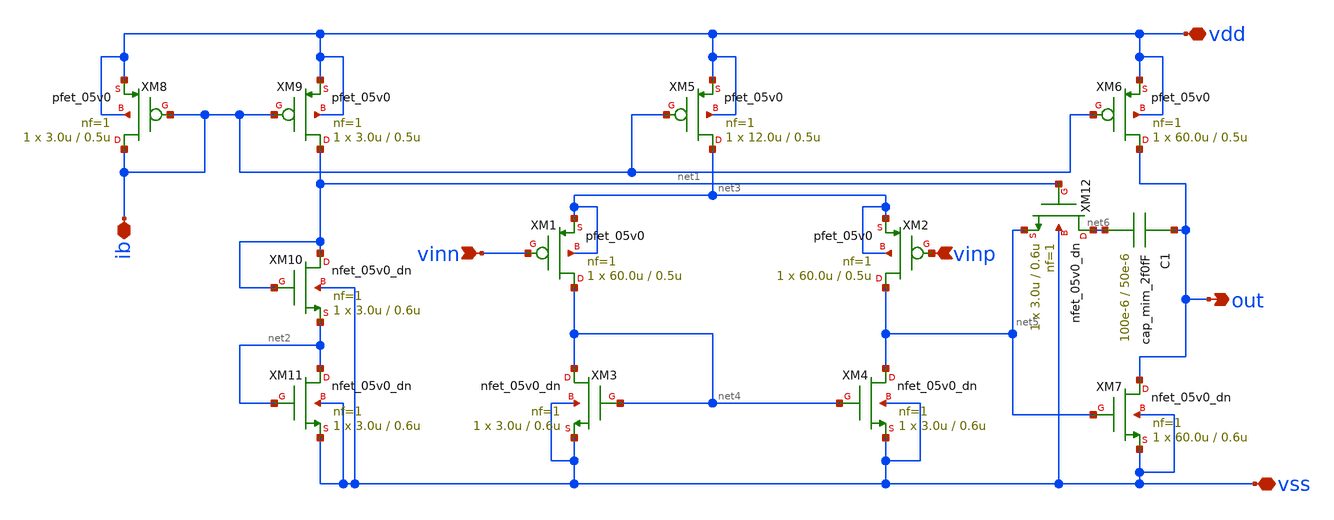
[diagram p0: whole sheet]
** sch_path: member_project/yamada3/opamp_2L_5V.sch
**.subckt opamp_2L_5V ib vdd vinn out vss vinp
*.iopin ib
*.iopin vdd
*.ipin vinn
*.opin out
*.iopin vss
*.ipin vinp
XM1 net4 vinn net3 net3 pfet_05v0 L=0.5u W=60.0u nf=1 ad='int((nf+1)/2) * W/nf * 0.18u' as='int((nf+2)/2) * W/nf * 0.18u'
+ pd='2*int((nf+1)/2) * (W/nf + 0.18u)' ps='2*int((nf+2)/2) * (W/nf + 0.18u)' nrd='0.18u / W' nrs='0.18u / W'
+ sa=0 sb=0 sd=0 m=1
XM2 net5 vinp net3 net3 pfet_05v0 L=0.5u W=60.0u nf=1 ad='int((nf+1)/2) * W/nf * 0.18u' as='int((nf+2)/2) * W/nf * 0.18u'
+ pd='2*int((nf+1)/2) * (W/nf + 0.18u)' ps='2*int((nf+2)/2) * (W/nf + 0.18u)' nrd='0.18u / W' nrs='0.18u / W'
+ sa=0 sb=0 sd=0 m=1
XM5 net3 ib vdd vdd pfet_05v0 L=0.5u W=12.0u nf=1 ad='int((nf+1)/2) * W/nf * 0.18u' as='int((nf+2)/2) * W/nf * 0.18u'
+ pd='2*int((nf+1)/2) * (W/nf + 0.18u)' ps='2*int((nf+2)/2) * (W/nf + 0.18u)' nrd='0.18u / W' nrs='0.18u / W'
+ sa=0 sb=0 sd=0 m=1
XM6 out ib vdd vdd pfet_05v0 L=0.5u W=60.0u nf=1 ad='int((nf+1)/2) * W/nf * 0.18u' as='int((nf+2)/2) * W/nf * 0.18u'
+ pd='2*int((nf+1)/2) * (W/nf + 0.18u)' ps='2*int((nf+2)/2) * (W/nf + 0.18u)' nrd='0.18u / W' nrs='0.18u / W'
+ sa=0 sb=0 sd=0 m=1
XM9 net1 ib vdd vdd pfet_05v0 L=0.5u W=3.0u nf=1 ad='int((nf+1)/2) * W/nf * 0.18u' as='int((nf+2)/2) * W/nf * 0.18u'
+ pd='2*int((nf+1)/2) * (W/nf + 0.18u)' ps='2*int((nf+2)/2) * (W/nf + 0.18u)' nrd='0.18u / W' nrs='0.18u / W'
+ sa=0 sb=0 sd=0 m=1
XM8 ib ib vdd vdd pfet_05v0 L=0.5u W=3.0u nf=1 ad='int((nf+1)/2) * W/nf * 0.18u' as='int((nf+2)/2) * W/nf * 0.18u'
+ pd='2*int((nf+1)/2) * (W/nf + 0.18u)' ps='2*int((nf+2)/2) * (W/nf + 0.18u)' nrd='0.18u / W' nrs='0.18u / W'
+ sa=0 sb=0 sd=0 m=1
XM3 net4 net4 vss vss nfet_05v0_dn L=0.6u W=3.0u nf=1 ad='int((nf+1)/2) * W/nf * 0.18u' as='int((nf+2)/2) * W/nf * 0.18u'
+ pd='2*int((nf+1)/2) * (W/nf + 0.18u)' ps='2*int((nf+2)/2) * (W/nf + 0.18u)' nrd='0.18u / W' nrs='0.18u / W'
+ sa=0 sb=0 sd=0 m=1
XM4 net5 net4 vss vss nfet_05v0_dn L=0.6u W=3.0u nf=1 ad='int((nf+1)/2) * W/nf * 0.18u' as='int((nf+2)/2) * W/nf * 0.18u'
+ pd='2*int((nf+1)/2) * (W/nf + 0.18u)' ps='2*int((nf+2)/2) * (W/nf + 0.18u)' nrd='0.18u / W' nrs='0.18u / W'
+ sa=0 sb=0 sd=0 m=1
XM7 out net5 vss vss nfet_05v0_dn L=0.6u W=60.0u nf=1 ad='int((nf+1)/2) * W/nf * 0.18u' as='int((nf+2)/2) * W/nf * 0.18u'
+ pd='2*int((nf+1)/2) * (W/nf + 0.18u)' ps='2*int((nf+2)/2) * (W/nf + 0.18u)' nrd='0.18u / W' nrs='0.18u / W'
+ sa=0 sb=0 sd=0 m=1
XM12 net6 net1 net5 vss nfet_05v0_dn L=0.6u W=3.0u nf=1 ad='int((nf+1)/2) * W/nf * 0.18u' as='int((nf+2)/2) * W/nf * 0.18u'
+ pd='2*int((nf+1)/2) * (W/nf + 0.18u)' ps='2*int((nf+2)/2) * (W/nf + 0.18u)' nrd='0.18u / W' nrs='0.18u / W'
+ sa=0 sb=0 sd=0 m=1
XM10 net1 net1 net2 vss nfet_05v0_dn L=0.6u W=3.0u nf=1 ad='int((nf+1)/2) * W/nf * 0.18u' as='int((nf+2)/2) * W/nf * 0.18u'
+ pd='2*int((nf+1)/2) * (W/nf + 0.18u)' ps='2*int((nf+2)/2) * (W/nf + 0.18u)' nrd='0.18u / W' nrs='0.18u / W'
+ sa=0 sb=0 sd=0 m=1
XM11 net2 net2 vss vss nfet_05v0_dn L=0.6u W=3.0u nf=1 ad='int((nf+1)/2) * W/nf * 0.18u' as='int((nf+2)/2) * W/nf * 0.18u'
+ pd='2*int((nf+1)/2) * (W/nf + 0.18u)' ps='2*int((nf+2)/2) * (W/nf + 0.18u)' nrd='0.18u / W' nrs='0.18u / W'
+ sa=0 sb=0 sd=0 m=1
C1 out net6 cap_mim_2f0fF W=100e-6 L=50e-6
**.ends
.end
